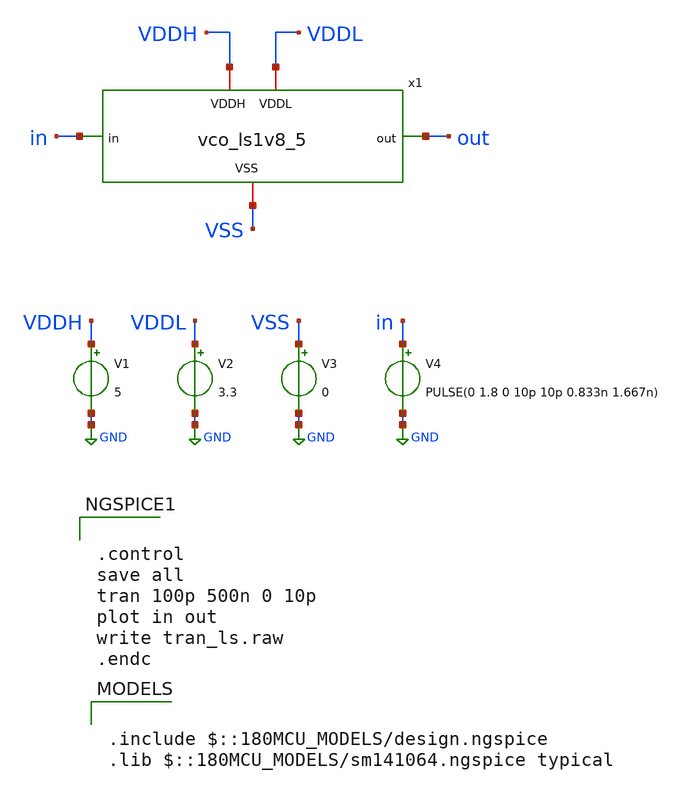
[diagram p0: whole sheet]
** sch_path: designs/libs/tb_vco/tb_vco_ls1v8_5/tb_vco_ls1v8_5.sch
**.subckt tb_vco_ls1v8_5
V1 VDDH GND 5
V3 VSS GND 0
V2 VDDL GND 3.3
x1 VSS VDDH VDDL out in vco_ls1v8_5
V4 in GND PULSE(0 1.8 0 10p 10p 0.833n 1.667n)
**** begin user architecture code

.include $::180MCU_MODELS/design.ngspice
.lib $::180MCU_MODELS/sm141064.ngspice typical



.control
save all
tran 100p 500n 0 10p
plot in out
write tran_ls.raw
.endc


**** end user architecture code
**.ends

* expanding   symbol:  libs/core_vco/vco_ls1v8_5/vco_ls1v8_5.sym # of pins=5
** sym_path: designs/libs/core_vco/vco_ls1v8_5/vco_ls1v8_5.sym
** sch_path: designs/libs/core_vco/vco_ls1v8_5/vco_ls1v8_5.sch
.subckt vco_ls1v8_5 VSS VDDH VDDL out in
*.iopin VDDH
*.iopin VDDL
*.opin out
*.iopin VSS
*.ipin in
XM1 net2 net1 VDDH VDDH pfet_05v0 L=0.5u W=0.3u nf=1 ad='int((nf+1)/2) * W/nf * 0.18u' as='int((nf+2)/2) * W/nf * 0.18u'
+ pd='2*int((nf+1)/2) * (W/nf + 0.18u)' ps='2*int((nf+2)/2) * (W/nf + 0.18u)' nrd='0.18u / W' nrs='0.18u / W'
+ sa=0 sb=0 sd=0 m=1
XM2 net1 net2 VDDH VDDH pfet_05v0 L=0.5u W=0.3u nf=1 ad='int((nf+1)/2) * W/nf * 0.18u' as='int((nf+2)/2) * W/nf * 0.18u'
+ pd='2*int((nf+1)/2) * (W/nf + 0.18u)' ps='2*int((nf+2)/2) * (W/nf + 0.18u)' nrd='0.18u / W' nrs='0.18u / W'
+ sa=0 sb=0 sd=0 m=1
XM3 net1 in VSS VSS nfet_05v0 L=0.6u W=0.6u nf=1 ad='int((nf+1)/2) * W/nf * 0.18u' as='int((nf+2)/2) * W/nf * 0.18u'
+ pd='2*int((nf+1)/2) * (W/nf + 0.18u)' ps='2*int((nf+2)/2) * (W/nf + 0.18u)' nrd='0.18u / W' nrs='0.18u / W'
+ sa=0 sb=0 sd=0 m=1
XM4 net2 net3 VSS VSS nfet_05v0 L=0.6u W=0.6u nf=1 ad='int((nf+1)/2) * W/nf * 0.18u' as='int((nf+2)/2) * W/nf * 0.18u'
+ pd='2*int((nf+1)/2) * (W/nf + 0.18u)' ps='2*int((nf+2)/2) * (W/nf + 0.18u)' nrd='0.18u / W' nrs='0.18u / W'
+ sa=0 sb=0 sd=0 m=1
XM5 net3 in VSS VSS nfet_03v3 L=0.28u W=1.5u nf=1 ad='int((nf+1)/2) * W/nf * 0.18u' as='int((nf+2)/2) * W/nf * 0.18u'
+ pd='2*int((nf+1)/2) * (W/nf + 0.18u)' ps='2*int((nf+2)/2) * (W/nf + 0.18u)' nrd='0.18u / W' nrs='0.18u / W'
+ sa=0 sb=0 sd=0 m=1
XM6 net3 in VDDL VDDL pfet_03v3 L=3u W=0.3u nf=1 ad='int((nf+1)/2) * W/nf * 0.18u' as='int((nf+2)/2) * W/nf * 0.18u'
+ pd='2*int((nf+1)/2) * (W/nf + 0.18u)' ps='2*int((nf+2)/2) * (W/nf + 0.18u)' nrd='0.18u / W' nrs='0.18u / W'
+ sa=0 sb=0 sd=0 m=1
XM7 net4 net2 VDDH VDDH pfet_05v0 L=0.6u W=1u nf=1 ad='int((nf+1)/2) * W/nf * 0.18u' as='int((nf+2)/2) * W/nf * 0.18u'
+ pd='2*int((nf+1)/2) * (W/nf + 0.18u)' ps='2*int((nf+2)/2) * (W/nf + 0.18u)' nrd='0.18u / W' nrs='0.18u / W'
+ sa=0 sb=0 sd=0 m=1
XM8 net4 net2 VSS VSS nfet_05v0 L=0.6u W=1u nf=2 ad='int((nf+1)/2) * W/nf * 0.18u' as='int((nf+2)/2) * W/nf * 0.18u'
+ pd='2*int((nf+1)/2) * (W/nf + 0.18u)' ps='2*int((nf+2)/2) * (W/nf + 0.18u)' nrd='0.18u / W' nrs='0.18u / W'
+ sa=0 sb=0 sd=0 m=1
XM9 net5 net4 VDDH VDDH pfet_05v0 L=0.6u W=1u nf=1 ad='int((nf+1)/2) * W/nf * 0.18u' as='int((nf+2)/2) * W/nf * 0.18u'
+ pd='2*int((nf+1)/2) * (W/nf + 0.18u)' ps='2*int((nf+2)/2) * (W/nf + 0.18u)' nrd='0.18u / W' nrs='0.18u / W'
+ sa=0 sb=0 sd=0 m=1
XM12 net6 net5 VDDH VDDH pfet_05v0 L=0.6u W=1u nf=1 ad='int((nf+1)/2) * W/nf * 0.18u' as='int((nf+2)/2) * W/nf * 0.18u'
+ pd='2*int((nf+1)/2) * (W/nf + 0.18u)' ps='2*int((nf+2)/2) * (W/nf + 0.18u)' nrd='0.18u / W' nrs='0.18u / W'
+ sa=0 sb=0 sd=0 m=1
XM14 out net6 VDDH VDDH pfet_05v0 L=0.6u W=1u nf=1 ad='int((nf+1)/2) * W/nf * 0.18u' as='int((nf+2)/2) * W/nf * 0.18u'
+ pd='2*int((nf+1)/2) * (W/nf + 0.18u)' ps='2*int((nf+2)/2) * (W/nf + 0.18u)' nrd='0.18u / W' nrs='0.18u / W'
+ sa=0 sb=0 sd=0 m=1
XM10 net5 net4 VSS VSS nfet_05v0 L=0.6u W=1u nf=2 ad='int((nf+1)/2) * W/nf * 0.18u' as='int((nf+2)/2) * W/nf * 0.18u'
+ pd='2*int((nf+1)/2) * (W/nf + 0.18u)' ps='2*int((nf+2)/2) * (W/nf + 0.18u)' nrd='0.18u / W' nrs='0.18u / W'
+ sa=0 sb=0 sd=0 m=1
XM11 net6 net5 VSS VSS nfet_05v0 L=0.6u W=1u nf=2 ad='int((nf+1)/2) * W/nf * 0.18u' as='int((nf+2)/2) * W/nf * 0.18u'
+ pd='2*int((nf+1)/2) * (W/nf + 0.18u)' ps='2*int((nf+2)/2) * (W/nf + 0.18u)' nrd='0.18u / W' nrs='0.18u / W'
+ sa=0 sb=0 sd=0 m=1
XM13 out net6 VSS VSS nfet_05v0 L=0.6u W=1u nf=2 ad='int((nf+1)/2) * W/nf * 0.18u' as='int((nf+2)/2) * W/nf * 0.18u'
+ pd='2*int((nf+1)/2) * (W/nf + 0.18u)' ps='2*int((nf+2)/2) * (W/nf + 0.18u)' nrd='0.18u / W' nrs='0.18u / W'
+ sa=0 sb=0 sd=0 m=1
.ends

.GLOBAL GND
.end
